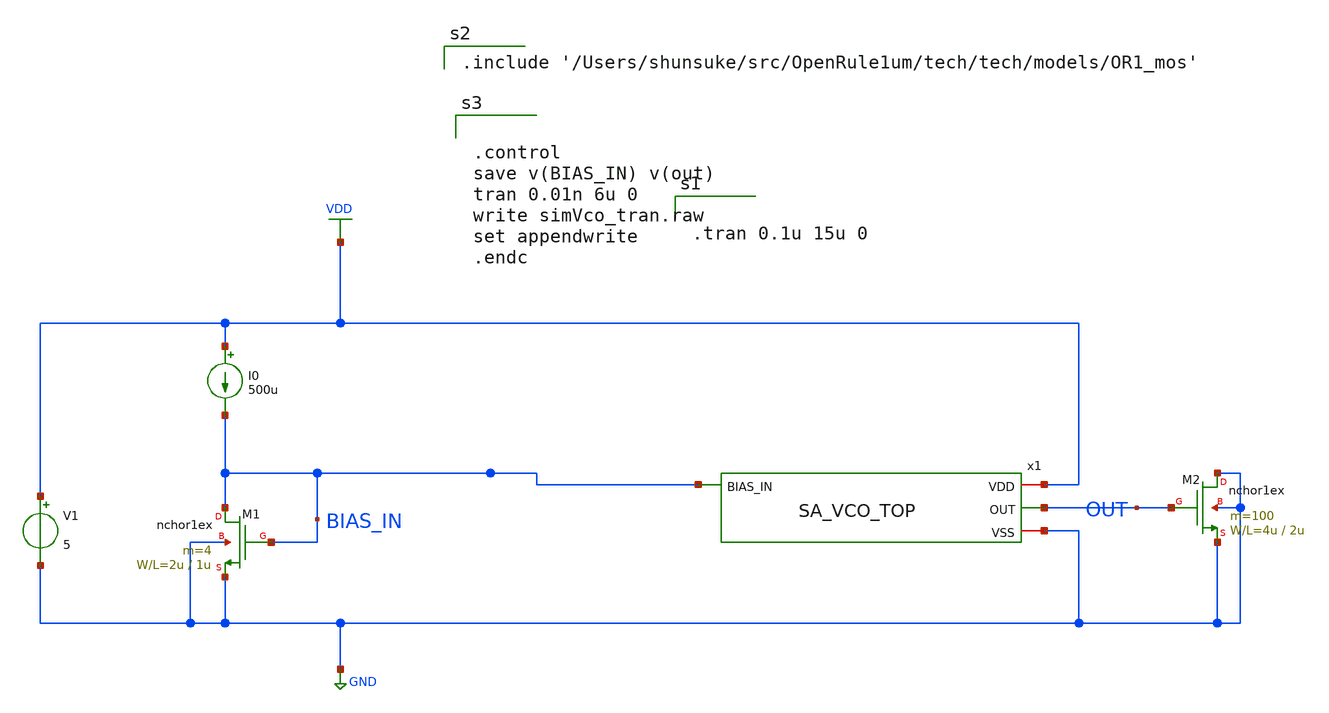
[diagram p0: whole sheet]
** sch_path: design/xschem/testbench/testVco.sch
**.subckt testVco
V1 VDD GND 5
.save i(v1)
M1 BIAS_IN BIAS_IN GND GND nchor1ex L=1u W=2u m=4
I0 VDD BIAS_IN 500u
x1 VDD BIAS_IN OUT GND SA_VCO_TOP
M2 GND OUT GND GND nchor1ex L=2u W=4u m=100
**** begin user architecture code


.tran 0.1u 15u 0



.include '/Users/shunsuke/src/OpenRule1um/tech/tech/models/OR1_mos'



.control
save v(BIAS_IN) v(out)
tran 0.01n 6u 0
write simVco_tran.raw
set appendwrite
.endc


**** end user architecture code
**.ends

* expanding   symbol:  VCO/SA_VCO_TOP.sym # of pins=4
** sym_path: design/xschem/VCO/SA_VCO_TOP.sym
** sch_path: design/xschem/VCO/SA_VCO_TOP.sch
.subckt SA_VCO_TOP VDD BIAS_IN OUT VSS
*.ipin BIAS_IN
*.iopin VDD
*.iopin VSS
*.opin OUT
x1 VDD O2D BIAS_IN VSS SA_VCO
x2 VDD VSS OUT O2D SA_DFF_Counter_8
.ends


* expanding   symbol:  VCO/SA_VCO.sym # of pins=4
** sym_path: design/xschem/VCO/SA_VCO.sym
** sch_path: design/xschem/VCO/SA_VCO.sch
.subckt SA_VCO VDD OUT BIAS_IN VSS
*.iopin VDD
*.iopin VSS
*.ipin BIAS_IN
*.opin OUT
x1 VDD VDD VSS net1 OUT RO_9
M1 net1 BIAS_IN VSS VSS nchor1ex L=1u W=2u m=4
M2 VSS VSS VSS VSS nchor1ex L=1u W=2u m=2
.ends


* expanding   symbol:  VCO/SA_DFF_Counter_8.sym # of pins=4
** sym_path: design/xschem/VCO/SA_DFF_Counter_8.sym
** sch_path: design/xschem/VCO/SA_DFF_Counter_8.sch
.subckt SA_DFF_Counter_8 VDD VSS OUT IN
*.ipin IN
*.iopin VDD
*.iopin VSS
*.opin OUT
x1 VDD VSS net1 IN SA_DFF_Counter
x2 VDD VSS net2 net1 SA_DFF_Counter
x3 VDD VSS net3 net2 SA_DFF_Counter
x4 VDD VSS net4 net3 SA_DFF_Counter
x5 VDD VSS net5 net4 SA_DFF_Counter
x6 VDD VSS net6 net5 SA_DFF_Counter
x7 VDD VSS net7 net6 SA_DFF_Counter
x8 VDD VSS OUT net7 SA_DFF_Counter
.ends


* expanding   symbol:  VCO/RO_9.sym # of pins=5
** sym_path: design/.design_bk/xschem/VCO/RO_9.sym
** sch_path: design/.design_bk/xschem/VCO/RO_9.sch
.subckt RO_9 pchSource VDD VSS nchSource OUT
*.iopin pchSource
*.iopin VDD
*.iopin VSS
*.iopin nchSource
*.opin OUT
x2 VDD net1 net2 VSS nchSource SA_VCO_INV
x3 VDD net2 net3 VSS nchSource SA_VCO_INV
x4 VDD net3 net4 VSS nchSource SA_VCO_INV
x5 VDD net4 net5 VSS nchSource SA_VCO_INV
x6 VDD net5 net6 VSS nchSource SA_VCO_INV
x7 VDD net6 net7 VSS nchSource SA_VCO_INV
x8 VDD net7 net8 VSS nchSource SA_VCO_INV
x9 VDD net8 net10 VSS nchSource SA_VCO_INV
x10 VDD net8 OUT VSS VSS SA_VCO_INV
x1 VDD net9 net1 VSS nchSource SA_VCO_INV
x11 VDD net10 net11 VSS nchSource SA_VCO_INV
x12 VDD net11 net12 VSS nchSource SA_VCO_INV
x13 VDD net12 net13 VSS nchSource SA_VCO_INV
x14 VDD net13 net14 VSS nchSource SA_VCO_INV
x15 VDD net14 net15 VSS nchSource SA_VCO_INV
x16 VDD net15 net16 VSS nchSource SA_VCO_INV
x17 VDD net16 net17 VSS nchSource SA_VCO_INV
x18 VDD net17 net9 VSS nchSource SA_VCO_INV
.ends


* expanding   symbol:  VCO/SA_DFF_Counter.sym # of pins=4
** sym_path: design/xschem/VCO/SA_DFF_Counter.sym
** sch_path: design/xschem/VCO/SA_DFF_Counter.sch
.subckt SA_DFF_Counter VDD VSS OUT IN
*.ipin IN
*.iopin VDD
*.iopin VSS
*.opin OUT
x2 IN IN net1 VDD VSS OUT net1 dff1
.ends


* expanding   symbol:  VCO/SA_VCO_INV.sym # of pins=5
** sym_path: design/xschem/VCO/SA_VCO_INV.sym
** sch_path: design/xschem/VCO/SA_VCO_INV.sch
.subckt SA_VCO_INV VDD IN OUT VSS nchSource
*.iopin nchSource
*.ipin IN
*.opin OUT
*.iopin VDD
*.iopin VSS
M1 VSS OUT VSS VSS nchor1ex L=3u W=6u m=1
M2 OUT IN VDD VDD pchor1ex L=1u W=4u m=4
M3 OUT IN nchSource VSS nchor1ex L=1u W=4u m=2
.ends

.GLOBAL VDD
.GLOBAL GND
.end
